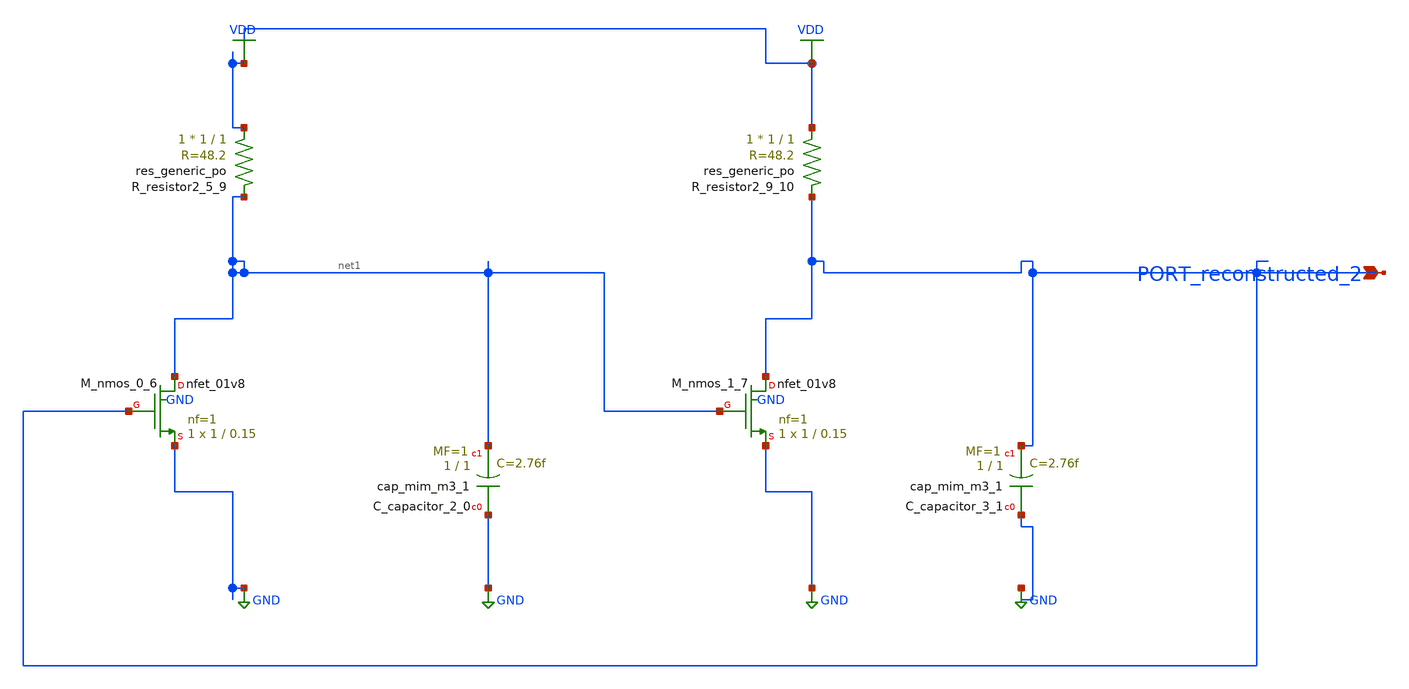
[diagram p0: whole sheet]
** sch_path: schematics/AMSNet/819.sch
**.subckt 819 PORT_reconstructed_2
*.ipin PORT_reconstructed_2
XC_capacitor_2_0 GND net1 sky130_fd_pr__cap_mim_m3_1 W=1 L=1 MF=1 m=1
XC_capacitor_3_1 GND PORT_reconstructed_2 sky130_fd_pr__cap_mim_m3_1 W=1 L=1 MF=1 m=1
XM_nmos_0_6 net1 PORT_reconstructed_2 GND GND sky130_fd_pr__nfet_01v8 L=0.15 W=1 nf=1 ad='int((1 + 1)/2) * 1 / 1 * 0.29'
+ as='int((1 + 2)/2) * 1 / 1 * 0.29' pd='2*int((1 + 1)/2) * (1 / 1 + 0.29)' ps='2*int((1 + 2)/2) * (1 / 1 + 0.29)'
+ nrd='0.29 / 1 ' nrs='0.29 / 1 ' sa=0 sb=0 sd=0 mult=1 m=1
XM_nmos_1_7 PORT_reconstructed_2 net1 GND GND sky130_fd_pr__nfet_01v8 L=0.15 W=1 nf=1 ad='int((1 + 1)/2) * 1 / 1 * 0.29'
+ as='int((1 + 2)/2) * 1 / 1 * 0.29' pd='2*int((1 + 1)/2) * (1 / 1 + 0.29)' ps='2*int((1 + 2)/2) * (1 / 1 + 0.29)'
+ nrd='0.29 / 1 ' nrs='0.29 / 1 ' sa=0 sb=0 sd=0 mult=1 m=1
XR_resistor2_5_9 VDD net1 sky130_fd_pr__res_generic_po W=1 L=1 m=1
XR_resistor2_9_10 VDD PORT_reconstructed_2 sky130_fd_pr__res_generic_po W=1 L=1 m=1
**.ends
.GLOBAL GND
.GLOBAL VDD
.end
